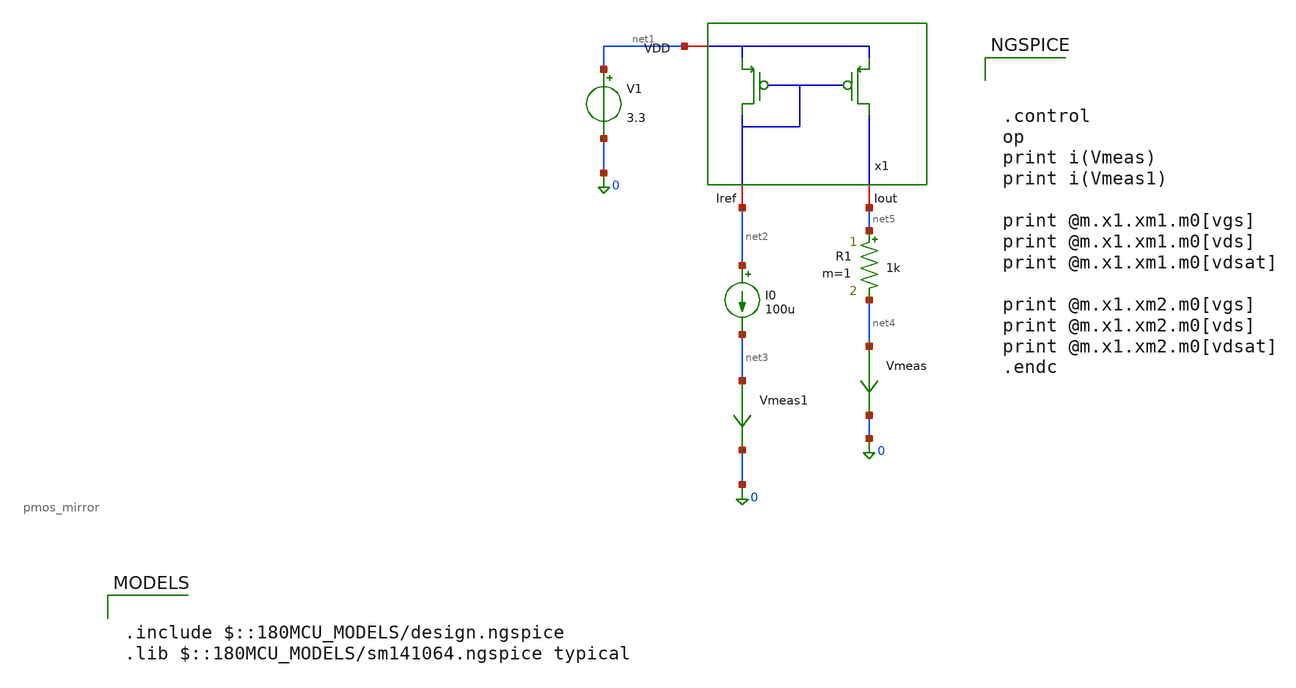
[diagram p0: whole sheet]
** sch_path: designs/mirrors/testbench/pmos_mirror_tb.sch
**.subckt pmos_mirror_tb
x1 net1 net5 net2 pmos_mirror
V1 net1 0 3.3
I0 net2 net3 100u
R1 net5 net4 1k m=1
Vmeas net4 0 0
.save i(vmeas)
Vmeas1 net3 0 0
.save i(vmeas1)
**** begin user architecture code



.control
op
print i(Vmeas)
print i(Vmeas1)

print @m.x1.xm1.m0[vgs]
print @m.x1.xm1.m0[vds]
print @m.x1.xm1.m0[vdsat]

print @m.x1.xm2.m0[vgs]
print @m.x1.xm2.m0[vds]
print @m.x1.xm2.m0[vdsat]
.endc



.include $::180MCU_MODELS/design.ngspice
.lib $::180MCU_MODELS/sm141064.ngspice typical

**** end user architecture code
**.ends

* expanding   symbol:  /foss/designs/NYCMOS/designs/mirrors/schematic/pmos_mirror.sym # of pins=3
** sym_path: designs/mirrors/schematic/pmos_mirror.sym
** sch_path: designs/mirrors/schematic/pmos_mirror.sch
.subckt pmos_mirror VDD Iout Iref
*.iopin VDD
*.iopin Iref
*.iopin Iout
XM1 Iref Iref VDD VDD pfet_03v3 L=0.5u W=28u nf=7 ad='int((nf+1)/2) * W/nf * 0.18u' as='int((nf+2)/2) * W/nf * 0.18u'
+ pd='2*int((nf+1)/2) * (W/nf + 0.18u)' ps='2*int((nf+2)/2) * (W/nf + 0.18u)' nrd='0.18u / W' nrs='0.18u / W'
+ sa=0 sb=0 sd=0 m=1
XM2 Iout Iref VDD VDD pfet_03v3 L=0.5u W=56u nf=14 ad='int((nf+1)/2) * W/nf * 0.18u' as='int((nf+2)/2) * W/nf * 0.18u'
+ pd='2*int((nf+1)/2) * (W/nf + 0.18u)' ps='2*int((nf+2)/2) * (W/nf + 0.18u)' nrd='0.18u / W' nrs='0.18u / W'
+ sa=0 sb=0 sd=0 m=1
XM3 Iout Iref VDD VDD pfet_03v3 L=0.5u W=56u nf=14 ad='int((nf+1)/2) * W/nf * 0.18u' as='int((nf+2)/2) * W/nf * 0.18u'
+ pd='2*int((nf+1)/2) * (W/nf + 0.18u)' ps='2*int((nf+2)/2) * (W/nf + 0.18u)' nrd='0.18u / W' nrs='0.18u / W'
+ sa=0 sb=0 sd=0 m=1
.ends

.end
